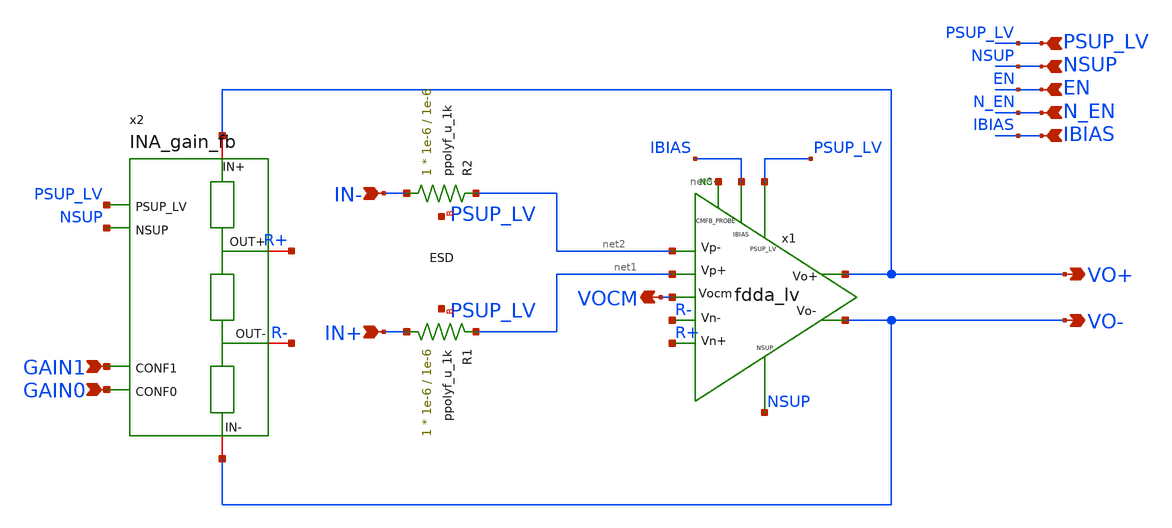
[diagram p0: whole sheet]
** sch_path: xschem/blocks/INA/INA.sch
**.subckt INA VO+ VO- NSUP EN N_EN IBIAS PSUP_LV GAIN0 GAIN1 VOCM IN- IN+
*.opin VO+
*.opin VO-
*.ipin NSUP
*.ipin EN
*.ipin N_EN
*.ipin IBIAS
*.ipin PSUP_LV
*.ipin GAIN0
*.ipin GAIN1
*.opin VOCM
*.ipin IN-
*.ipin IN+
* noconn #net3
x1 PSUP_LV net2 R- R+ net1 VO+ VO- IBIAS NSUP net3 VOCM fdda_lv
x2 VO+ R+ PSUP_LV NSUP GAIN1 GAIN0 R- VO- INA_gain_fb
XR2 IN- net2 PSUP_LV ppolyf_u_1k r_width=1e-6 r_length=1e-6 m=1
XR1 IN+ net1 PSUP_LV ppolyf_u_1k r_width=1e-6 r_length=1e-6 m=1
**.ends
.end
